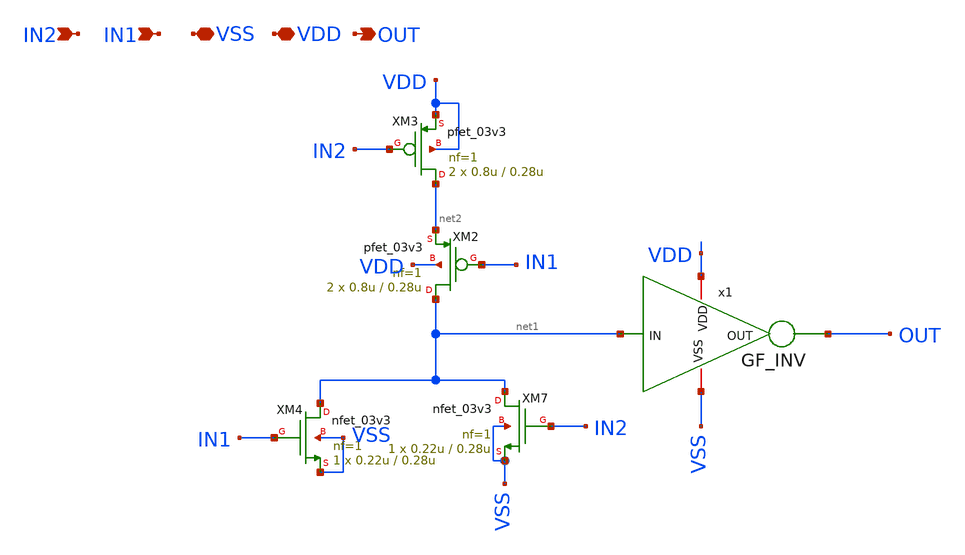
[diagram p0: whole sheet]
** sch_path: Clock_Generator_PAKISTAN_02/xschem/or_2.sch
**.subckt or_2 IN2 IN1 VSS VDD OUT
*.ipin IN2
*.ipin IN1
*.iopin VSS
*.iopin VDD
*.opin OUT
XM4 net1 IN1 VSS VSS nfet_03v3 L=0.28u W=0.22u nf=1 ad='int((nf+1)/2) * W/nf * 0.18u' as='int((nf+2)/2) * W/nf * 0.18u'
+ pd='2*int((nf+1)/2) * (W/nf + 0.18u)' ps='2*int((nf+2)/2) * (W/nf + 0.18u)' nrd='0.18u / W' nrs='0.18u / W'
+ sa=0 sb=0 sd=0 m=1
XM2 net1 IN1 net2 VDD pfet_03v3 L=0.28u W=0.8u nf=1 ad='int((nf+1)/2) * W/nf * 0.18u' as='int((nf+2)/2) * W/nf * 0.18u'
+ pd='2*int((nf+1)/2) * (W/nf + 0.18u)' ps='2*int((nf+2)/2) * (W/nf + 0.18u)' nrd='0.18u / W' nrs='0.18u / W'
+ sa=0 sb=0 sd=0 m=2
XM7 net1 IN2 VSS VSS nfet_03v3 L=0.28u W=0.22u nf=1 ad='int((nf+1)/2) * W/nf * 0.18u' as='int((nf+2)/2) * W/nf * 0.18u'
+ pd='2*int((nf+1)/2) * (W/nf + 0.18u)' ps='2*int((nf+2)/2) * (W/nf + 0.18u)' nrd='0.18u / W' nrs='0.18u / W'
+ sa=0 sb=0 sd=0 m=1
XM3 net2 IN2 VDD VDD pfet_03v3 L=0.28u W=0.8u nf=1 ad='int((nf+1)/2) * W/nf * 0.18u' as='int((nf+2)/2) * W/nf * 0.18u'
+ pd='2*int((nf+1)/2) * (W/nf + 0.18u)' ps='2*int((nf+2)/2) * (W/nf + 0.18u)' nrd='0.18u / W' nrs='0.18u / W'
+ sa=0 sb=0 sd=0 m=2
x1 VSS VDD OUT net1 GF_INV
**.ends

* expanding   symbol:  GF_INV.sym # of pins=4
** sym_path: GF_INV.sym
** sch_path: GF_INV.sch
.subckt GF_INV VSS VDD OUT IN
*.iopin VDD
*.iopin VSS
*.ipin IN
*.opin OUT
XM1 OUT IN VSS VSS nfet_03v3 L=0.56u W=0.56u nf=1 ad='int((nf+1)/2) * W/nf * 0.18u' as='int((nf+2)/2) * W/nf * 0.18u'
+ pd='2*int((nf+1)/2) * (W/nf + 0.18u)' ps='2*int((nf+2)/2) * (W/nf + 0.18u)' nrd='0.18u / W' nrs='0.18u / W'
+ sa=0 sb=0 sd=0 m=1
XM2 OUT IN VDD VDD pfet_03v3 L=0.56u W=1.12u nf=1 ad='int((nf+1)/2) * W/nf * 0.18u' as='int((nf+2)/2) * W/nf * 0.18u'
+ pd='2*int((nf+1)/2) * (W/nf + 0.18u)' ps='2*int((nf+2)/2) * (W/nf + 0.18u)' nrd='0.18u / W' nrs='0.18u / W'
+ sa=0 sb=0 sd=0 m=1
.ends

.end
